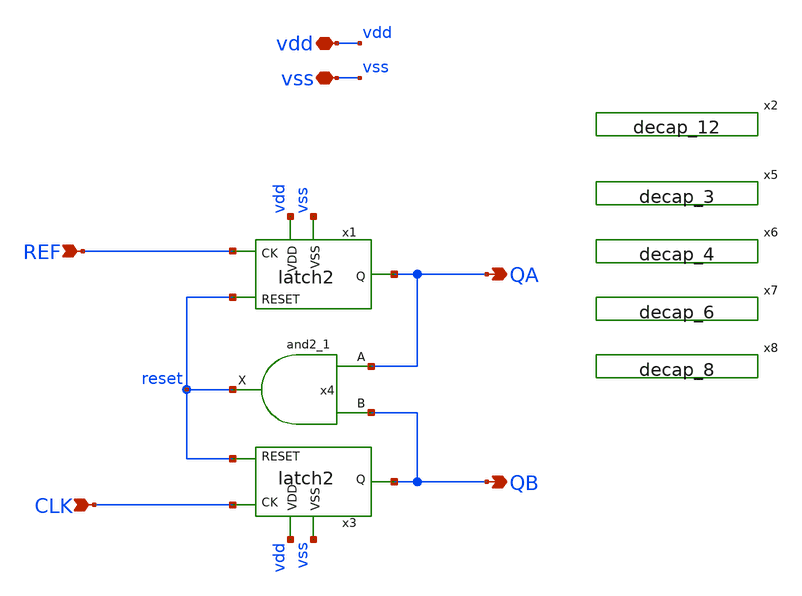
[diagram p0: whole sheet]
** sch_path: xschem/pfd.sch
**.subckt pfd vdd REF vss QA QB CLK
*.iopin vdd
*.ipin REF
*.iopin vss
*.opin QA
*.opin QB
*.ipin CLK
x1 REF QA reset vdd vss latch2
x3 CLK QB reset vdd vss latch2
x4 QA QB vss vss vdd vdd reset sky130_fd_sc_hd__and2_1
x2 vss vss vdd vdd sky130_fd_sc_hd__decap_12
x5 vss vss vdd vdd sky130_fd_sc_hd__decap_3
x6 vss vss vdd vdd sky130_fd_sc_hd__decap_4
x7 vss vss vdd vdd sky130_fd_sc_hd__decap_6
x8 vss vss vdd vdd sky130_fd_sc_hd__decap_8
**.ends

* expanding   symbol:  latch2.sym # of pins=5
** sym_path: xschem/latch2.sym
** sch_path: xschem/latch2.sch
.subckt latch2 CK Q RESET VDD VSS
*.ipin RESET
*.ipin CK
*.opin Q
*.ipin VDD
*.ipin VSS
x1 net3 net2 VSS VSS VDD VDD net1 sky130_fd_sc_hd__nor2_1
x2 net1 RESET VSS VSS VDD VDD net2 sky130_fd_sc_hd__nor2_1
x3 CK Q VSS VSS VDD VDD net3 sky130_fd_sc_hd__nor2_1
x4 net3 net1 VSS VSS VDD VDD Q sky130_fd_sc_hd__nor2_4
.ends

.end
